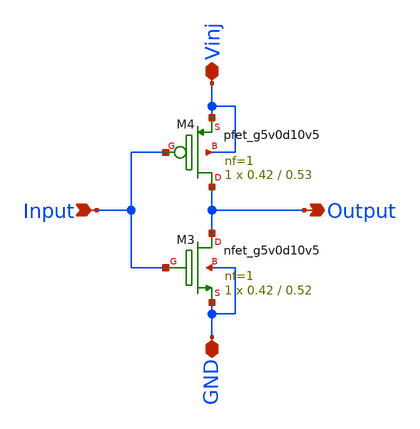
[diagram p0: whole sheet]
** sch_path: sky130_cells/RDAC/Design/sky130_hilas_VinjInv2.sch
**.subckt sky130_hilas_VinjInv2 Input Output Vinj GND
*.ipin Input
*.opin Output
*.iopin Vinj
*.iopin GND
XM4 Output Input Vinj Vinj sky130_fd_pr__pfet_g5v0d10v5 L=0.53 W=0.42 nf=1 ad='int((nf+1)/2) * W/nf * 0.29'
+ as='int((nf+2)/2) * W/nf * 0.29' pd='2*int((nf+1)/2) * (W/nf + 0.29)' ps='2*int((nf+2)/2) * (W/nf + 0.29)'
+ nrd='0.29 / W' nrs='0.29 / W' sa=0 sb=0 sd=0 mult=1 m=1
XM3 Output Input GND GND sky130_fd_pr__nfet_g5v0d10v5 L=0.52 W=0.42 nf=1 ad='int((nf+1)/2) * W/nf * 0.29'
+ as='int((nf+2)/2) * W/nf * 0.29' pd='2*int((nf+1)/2) * (W/nf + 0.29)' ps='2*int((nf+2)/2) * (W/nf + 0.29)'
+ nrd='0.29 / W' nrs='0.29 / W' sa=0 sb=0 sd=0 mult=1 m=1
**.ends
.end
